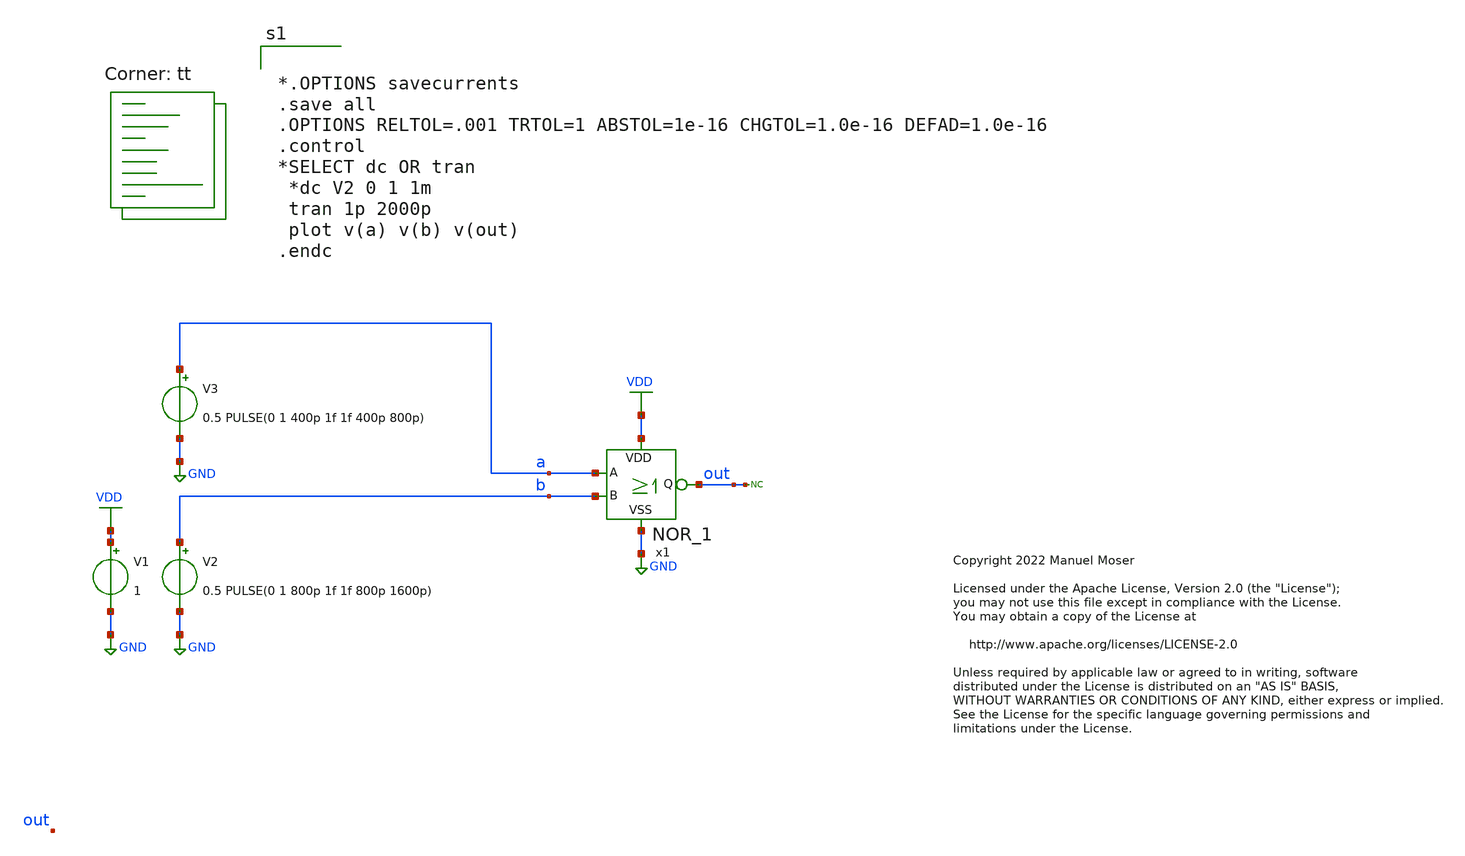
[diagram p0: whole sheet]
** sch_path: xschem/NOR/NOR_tb.sch
* Copyright 2022 Manuel Moser
* Licensed under the Apache License, Version 2.0 (the "License");
**.subckt NOR_tb
V1 VDD GND 1
x1 b a VDD out GND NOR_1
V3 a GND 0.5 PULSE(0 1 400p 1f 1f 400p 800p)
V2 b GND 0.5 PULSE(0 1 800p 1f 1f 800p 1600p)
* noconn out
**** begin user architecture code


*.OPTIONS savecurrents
.save all
.OPTIONS RELTOL=.001 TRTOL=1 ABSTOL=1e-16 CHGTOL=1.0e-16 DEFAD=1.0e-16
.control
*SELECT dc OR tran
 *dc V2 0 1 1m
 tran 1p 2000p
 plot v(a) v(b) v(out)
.endc


.lib $::SKYWATER_MODELS/sky130.lib.spice tt
**** end user architecture code
**.ends

* expanding   symbol:  NOR_1.sym # of pins=5
** sym_path: xschem/NOR/NOR_1.sym
** sch_path: xschem/NOR/NOR_1.sch
.subckt NOR_1 B A VDD Q VSS
*.iopin VDD
*.iopin VSS
*.ipin B
*.ipin A
*.opin Q
XM5 Q B VSS VSS sky130_fd_pr__nfet_01v8 L=0.15 W=0.42 nf=1 ad='int((nf+1)/2) * W/nf * 0.29' as='int((nf+2)/2) * W/nf * 0.29'
+ pd='2*int((nf+1)/2) * (W/nf + 0.29)' ps='2*int((nf+2)/2) * (W/nf + 0.29)' nrd='0.29 / W' nrs='0.29 / W'
+ sa=0 sb=0 sd=0 mult=1 m=1
XM6 Q A VSS VSS sky130_fd_pr__nfet_01v8 L=0.15 W=0.42 nf=1 ad='int((nf+1)/2) * W/nf * 0.29' as='int((nf+2)/2) * W/nf * 0.29'
+ pd='2*int((nf+1)/2) * (W/nf + 0.29)' ps='2*int((nf+2)/2) * (W/nf + 0.29)' nrd='0.29 / W' nrs='0.29 / W'
+ sa=0 sb=0 sd=0 mult=1 m=1
XM1 Q B net1 VDD sky130_fd_pr__pfet_01v8 L=0.15 W=0.8 nf=1 ad='int((nf+1)/2) * W/nf * 0.29' as='int((nf+2)/2) * W/nf * 0.29'
+ pd='2*int((nf+1)/2) * (W/nf + 0.29)' ps='2*int((nf+2)/2) * (W/nf + 0.29)' nrd='0.29 / W' nrs='0.29 / W'
+ sa=0 sb=0 sd=0 mult=1 m=1
XM2 Q A net2 VDD sky130_fd_pr__pfet_01v8 L=0.15 W=0.8 nf=1 ad='int((nf+1)/2) * W/nf * 0.29' as='int((nf+2)/2) * W/nf * 0.29'
+ pd='2*int((nf+1)/2) * (W/nf + 0.29)' ps='2*int((nf+2)/2) * (W/nf + 0.29)' nrd='0.29 / W' nrs='0.29 / W'
+ sa=0 sb=0 sd=0 mult=1 m=1
XM3 net2 B VDD VDD sky130_fd_pr__pfet_01v8 L=0.15 W=0.8 nf=1 ad='int((nf+1)/2) * W/nf * 0.29' as='int((nf+2)/2) * W/nf * 0.29'
+ pd='2*int((nf+1)/2) * (W/nf + 0.29)' ps='2*int((nf+2)/2) * (W/nf + 0.29)' nrd='0.29 / W' nrs='0.29 / W'
+ sa=0 sb=0 sd=0 mult=1 m=1
XM4 net1 A VDD VDD sky130_fd_pr__pfet_01v8 L=0.15 W=0.8 nf=1 ad='int((nf+1)/2) * W/nf * 0.29' as='int((nf+2)/2) * W/nf * 0.29'
+ pd='2*int((nf+1)/2) * (W/nf + 0.29)' ps='2*int((nf+2)/2) * (W/nf + 0.29)' nrd='0.29 / W' nrs='0.29 / W'
+ sa=0 sb=0 sd=0 mult=1 m=1
.ends

.GLOBAL GND
.GLOBAL VDD
.end
